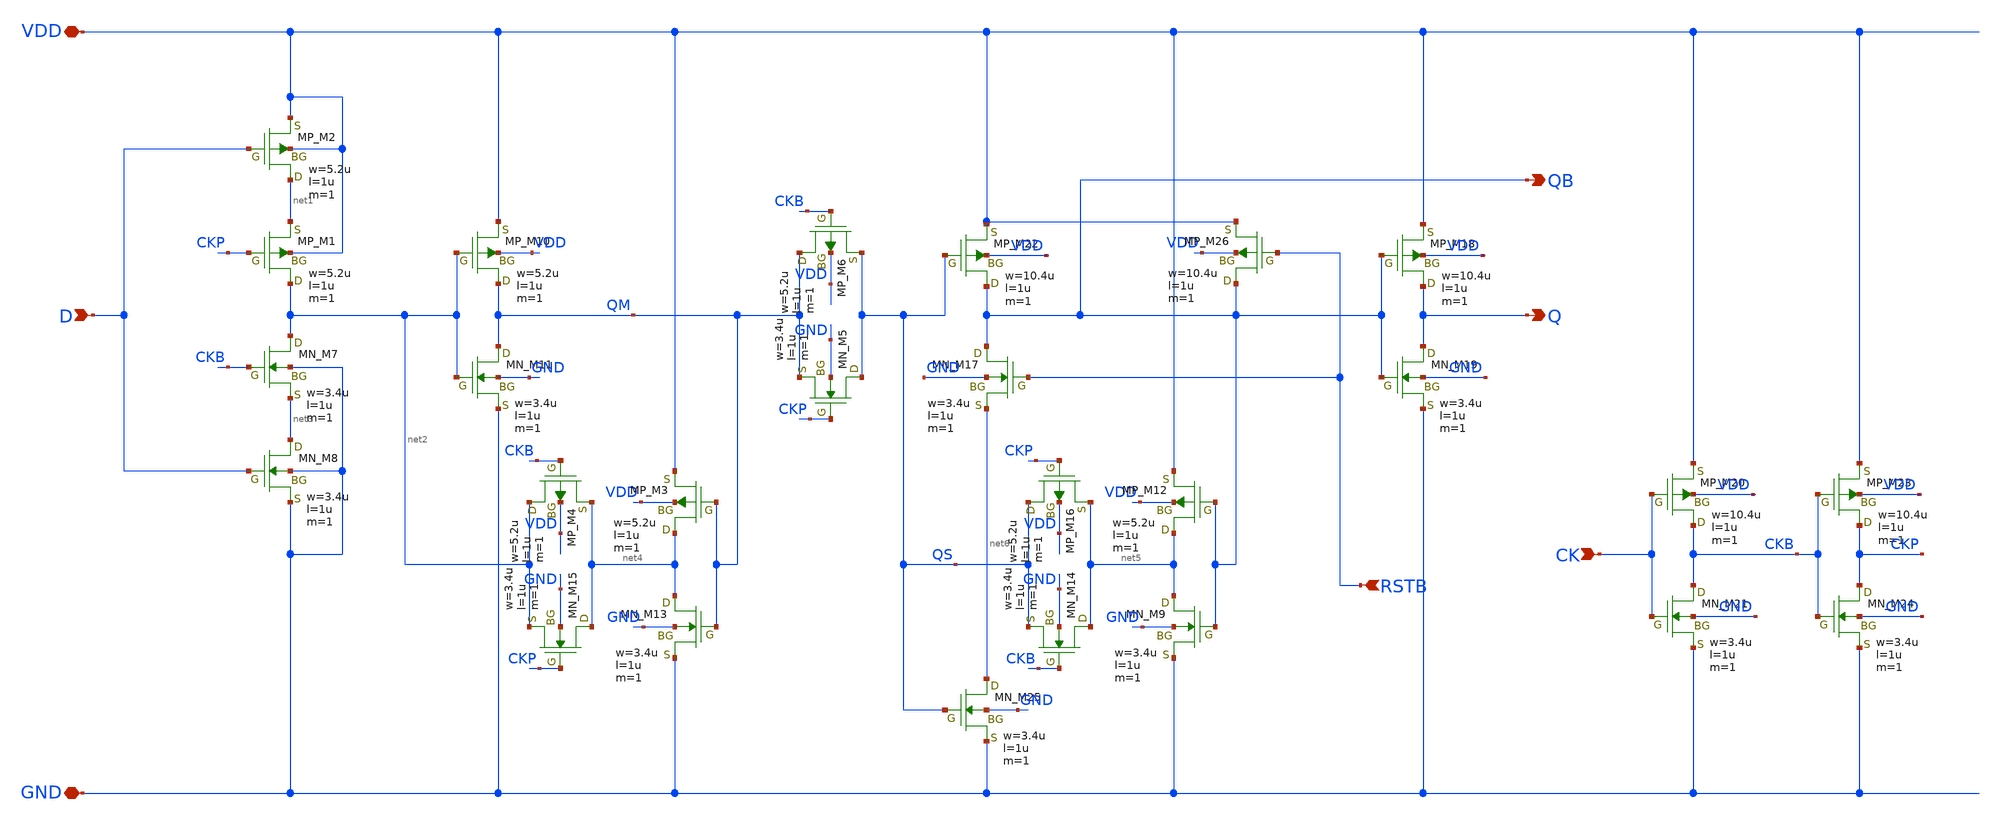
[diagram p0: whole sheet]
** sch_path: LEF/DFFR.sch
**.subckt DFFR VDD GND D QB CK Q RSTB
*.iopin VDD
*.iopin GND
*.ipin D
*.opin QB
*.ipin CK
*.opin Q
*.ipin RSTB
XM2 net1 D VDD VDD PMOS w=5.2u l=1u as=0 ad=0 ps=0 pd=0 nrd=0 nrs=0 m=1
XM1 net2 CKP net1 VDD PMOS w=5.2u l=1u as=0 ad=0 ps=0 pd=0 nrd=0 nrs=0 m=1
XM7 net2 CKB net3 GND NMOS w=3.4u l=1u as=0 ad=0 ps=0 pd=0 nrd=0 nrs=0 m=1
XM8 net3 D GND GND NMOS w=3.4u l=1u as=0 ad=0 ps=0 pd=0 nrd=0 nrs=0 m=1
XM10 QM net2 VDD VDD PMOS w=5.2u l=1u as=0 ad=0 ps=0 pd=0 nrd=0 nrs=0 m=1
XM11 QM net2 GND GND NMOS w=3.4u l=1u as=0 ad=0 ps=0 pd=0 nrd=0 nrs=0 m=1
XM13 net4 QM GND GND NMOS w=3.4u l=1u as=0 ad=0 ps=0 pd=0 nrd=0 nrs=0 m=1
XM15 net4 CKP net2 GND NMOS w=3.4u l=1u as=0 ad=0 ps=0 pd=0 nrd=0 nrs=0 m=1
XM22 QB QS VDD VDD PMOS w=10.4u l=1u as=0 ad=0 ps=0 pd=0 nrd=0 nrs=0 m=1
XM3 net4 QM VDD VDD PMOS w=5.2u l=1u as=0 ad=0 ps=0 pd=0 nrd=0 nrs=0 m=1
XM4 net2 CKB net4 VDD PMOS w=5.2u l=1u as=0 ad=0 ps=0 pd=0 nrd=0 nrs=0 m=1
XM5 QS CKP QM GND NMOS w=3.4u l=1u as=0 ad=0 ps=0 pd=0 nrd=0 nrs=0 m=1
XM6 QM CKB QS VDD PMOS w=5.2u l=1u as=0 ad=0 ps=0 pd=0 nrd=0 nrs=0 m=1
XM9 net5 QB GND GND NMOS w=3.4u l=1u as=0 ad=0 ps=0 pd=0 nrd=0 nrs=0 m=1
XM12 net5 QB VDD VDD PMOS w=5.2u l=1u as=0 ad=0 ps=0 pd=0 nrd=0 nrs=0 m=1
XM14 net5 CKB QS GND NMOS w=3.4u l=1u as=0 ad=0 ps=0 pd=0 nrd=0 nrs=0 m=1
XM16 QS CKP net5 VDD PMOS w=5.2u l=1u as=0 ad=0 ps=0 pd=0 nrd=0 nrs=0 m=1
XM17 QB RSTB net6 GND NMOS w=3.4u l=1u as=0 ad=0 ps=0 pd=0 nrd=0 nrs=0 m=1
XM18 Q QB VDD VDD PMOS w=10.4u l=1u as=0 ad=0 ps=0 pd=0 nrd=0 nrs=0 m=1
XM19 Q QB GND GND NMOS w=3.4u l=1u as=0 ad=0 ps=0 pd=0 nrd=0 nrs=0 m=1
XM20 CKB CK VDD VDD PMOS w=10.4u l=1u as=0 ad=0 ps=0 pd=0 nrd=0 nrs=0 m=1
XM21 CKB CK GND GND NMOS w=3.4u l=1u as=0 ad=0 ps=0 pd=0 nrd=0 nrs=0 m=1
XM23 CKP CKB VDD VDD PMOS w=10.4u l=1u as=0 ad=0 ps=0 pd=0 nrd=0 nrs=0 m=1
XM24 CKP CKB GND GND NMOS w=3.4u l=1u as=0 ad=0 ps=0 pd=0 nrd=0 nrs=0 m=1
XM25 net6 QS GND GND NMOS w=3.4u l=1u as=0 ad=0 ps=0 pd=0 nrd=0 nrs=0 m=1
XM26 QB RSTB VDD VDD PMOS w=10.4u l=1u as=0 ad=0 ps=0 pd=0 nrd=0 nrs=0 m=1
**.ends
.end
